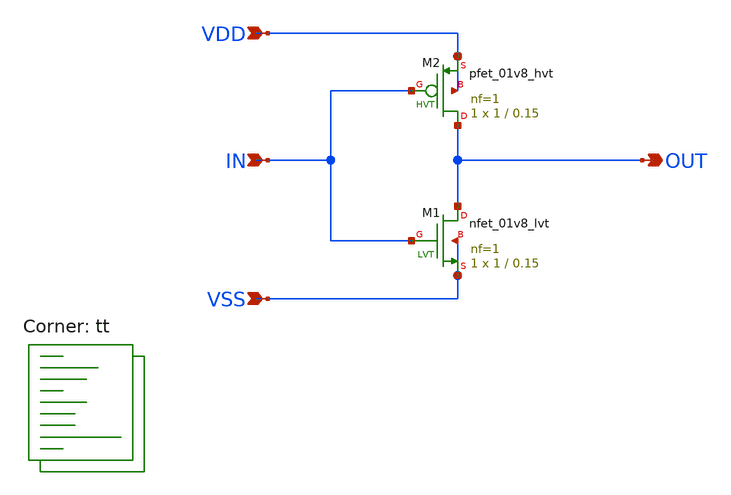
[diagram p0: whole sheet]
** sch_path: xscheme/INV.sch
**.subckt INV IN VSS VDD OUT
*.ipin IN
*.ipin VSS
*.ipin VDD
*.opin OUT
XM1 OUT IN VSS VSS sky130_fd_pr__nfet_01v8_lvt L=0.15 W=1 nf=1 ad='int((nf+1)/2) * W/nf * 0.29' as='int((nf+2)/2) * W/nf * 0.29'
+ pd='2*int((nf+1)/2) * (W/nf + 0.29)' ps='2*int((nf+2)/2) * (W/nf + 0.29)' nrd='0.29 / W' nrs='0.29 / W'
+ sa=0 sb=0 sd=0 mult=1 m=1
XM2 OUT IN VDD VDD sky130_fd_pr__pfet_01v8_hvt L=0.15 W=1 nf=1 ad='int((nf+1)/2) * W/nf * 0.29' as='int((nf+2)/2) * W/nf * 0.29'
+ pd='2*int((nf+1)/2) * (W/nf + 0.29)' ps='2*int((nf+2)/2) * (W/nf + 0.29)' nrd='0.29 / W' nrs='0.29 / W'
+ sa=0 sb=0 sd=0 mult=1 m=1
**** begin user architecture code
.lib $::SKYWATER_MODELS/sky130.lib.spice tt


.tran 10n 2000u uic
.save all


**** end user architecture code
**.ends
.end
